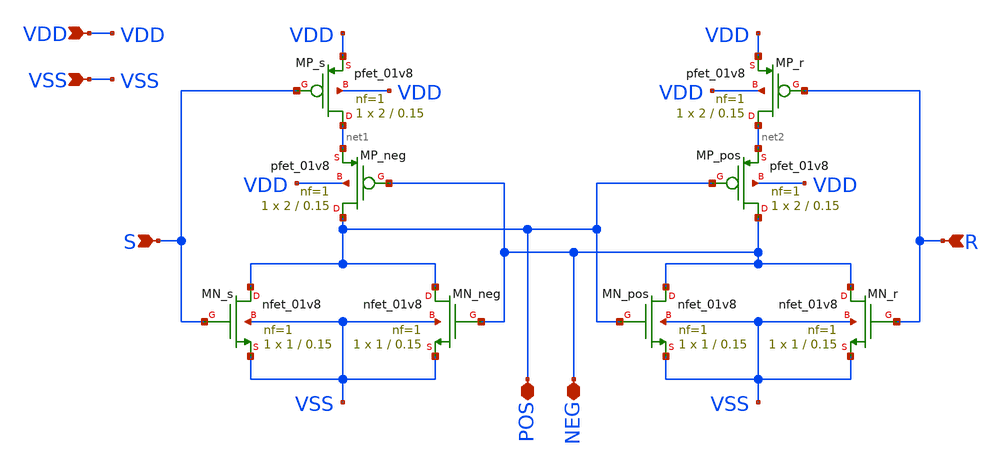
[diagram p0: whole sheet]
** sch_path: schem/symbol_repo/sym_sr_latch.sch
**.subckt sym_sr_latch S VDD R VSS POS NEG
*.ipin S
*.ipin VDD
*.ipin R
*.ipin VSS
*.iopin POS
*.iopin NEG
XMN_neg POS NEG VSS VSS sky130_fd_pr__nfet_01v8 L=0.15 W=1 nf=1 ad='int((1 + 1)/2) * 1 / 1 * 0.29' as='int((1 + 2)/2) * 1 / 1 * 0.29'
+ pd='2*int((1 + 1)/2) * (1 / 1 + 0.29)' ps='2*int((1 + 2)/2) * (1 / 1 + 0.29)' nrd='0.29 / 1 ' nrs='0.29 / 1 '
+ sa=0 sb=0 sd=0 mult=1 m=1
XMP_s net1 S VDD VDD sky130_fd_pr__pfet_01v8 L=0.15 W=2 nf=1 ad='int((1 + 1)/2) * 2 / 1 * 0.29' as='int((1 + 2)/2) * 2 / 1 * 0.29'
+ pd='2*int((1 + 1)/2) * (2 / 1 + 0.29)' ps='2*int((1 + 2)/2) * (2 / 1 + 0.29)' nrd='0.29 / 2 ' nrs='0.29 / 2 '
+ sa=0 sb=0 sd=0 mult=1 m=1
XMP_neg POS NEG net1 VDD sky130_fd_pr__pfet_01v8 L=0.15 W=2 nf=1 ad='int((1 + 1)/2) * 2 / 1 * 0.29' as='int((1 + 2)/2) * 2 / 1 * 0.29'
+ pd='2*int((1 + 1)/2) * (2 / 1 + 0.29)' ps='2*int((1 + 2)/2) * (2 / 1 + 0.29)' nrd='0.29 / 2 ' nrs='0.29 / 2 '
+ sa=0 sb=0 sd=0 mult=1 m=1
XMN_s POS S VSS VSS sky130_fd_pr__nfet_01v8 L=0.15 W=1 nf=1 ad='int((1 + 1)/2) * 1 / 1 * 0.29' as='int((1 + 2)/2) * 1 / 1 * 0.29'
+ pd='2*int((1 + 1)/2) * (1 / 1 + 0.29)' ps='2*int((1 + 2)/2) * (1 / 1 + 0.29)' nrd='0.29 / 1 ' nrs='0.29 / 1 '
+ sa=0 sb=0 sd=0 mult=1 m=1
XMN_r NEG R VSS VSS sky130_fd_pr__nfet_01v8 L=0.15 W=1 nf=1 ad='int((1 + 1)/2) * 1 / 1 * 0.29' as='int((1 + 2)/2) * 1 / 1 * 0.29'
+ pd='2*int((1 + 1)/2) * (1 / 1 + 0.29)' ps='2*int((1 + 2)/2) * (1 / 1 + 0.29)' nrd='0.29 / 1 ' nrs='0.29 / 1 '
+ sa=0 sb=0 sd=0 mult=1 m=1
XMP_r net2 R VDD VDD sky130_fd_pr__pfet_01v8 L=0.15 W=2 nf=1 ad='int((1 + 1)/2) * 2 / 1 * 0.29' as='int((1 + 2)/2) * 2 / 1 * 0.29'
+ pd='2*int((1 + 1)/2) * (2 / 1 + 0.29)' ps='2*int((1 + 2)/2) * (2 / 1 + 0.29)' nrd='0.29 / 2 ' nrs='0.29 / 2 '
+ sa=0 sb=0 sd=0 mult=1 m=1
XMP_pos NEG POS net2 VDD sky130_fd_pr__pfet_01v8 L=0.15 W=2 nf=1 ad='int((1 + 1)/2) * 2 / 1 * 0.29' as='int((1 + 2)/2) * 2 / 1 * 0.29'
+ pd='2*int((1 + 1)/2) * (2 / 1 + 0.29)' ps='2*int((1 + 2)/2) * (2 / 1 + 0.29)' nrd='0.29 / 2 ' nrs='0.29 / 2 '
+ sa=0 sb=0 sd=0 mult=1 m=1
XMN_pos NEG POS VSS VSS sky130_fd_pr__nfet_01v8 L=0.15 W=1 nf=1 ad='int((1 + 1)/2) * 1 / 1 * 0.29' as='int((1 + 2)/2) * 1 / 1 * 0.29'
+ pd='2*int((1 + 1)/2) * (1 / 1 + 0.29)' ps='2*int((1 + 2)/2) * (1 / 1 + 0.29)' nrd='0.29 / 1 ' nrs='0.29 / 1 '
+ sa=0 sb=0 sd=0 mult=1 m=1
**.ends
.end
